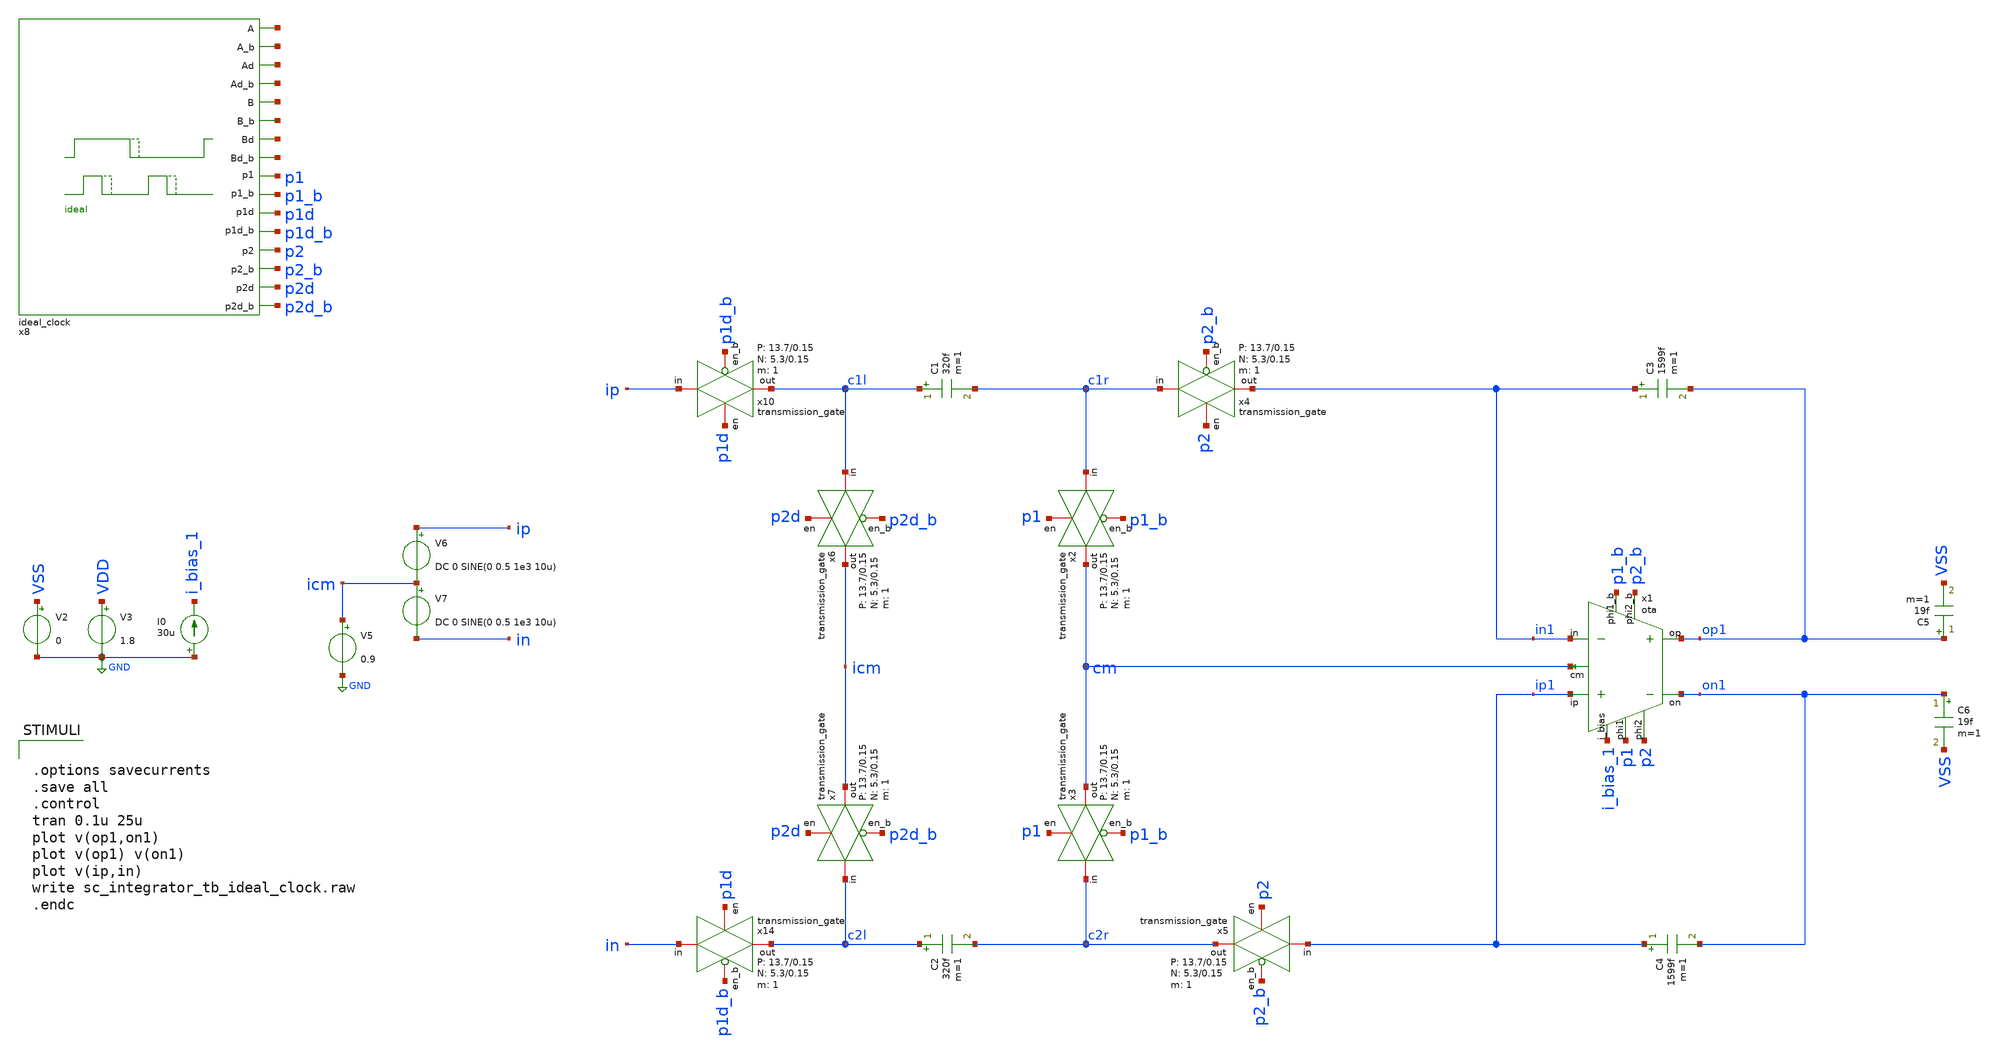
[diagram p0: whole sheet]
** sch_path: verification/analog_modulator/sc_integrator_tb_ideal_clock.sch
**.subckt sc_integrator_tb_ideal_clock
x4 c1r in1 p2 p2_b VDD VSS 1 5.3 0.15 13.7 0.15 transmission_gate
x5 ip1 c2r p2 p2_b VDD VSS 1 5.3 0.15 13.7 0.15 transmission_gate
x2 c1r cm p1 p1_b VDD VSS 1 5.3 0.15 13.7 0.15 transmission_gate
x3 c2r cm p1 p1_b VDD VSS 1 5.3 0.15 13.7 0.15 transmission_gate
C1 c1l c1r 320f m=1
C2 c2l c2r 320f m=1
x10 ip c1l p1d p1d_b VDD VSS 1 5.3 0.15 13.7 0.15 transmission_gate
x14 in c2l p1d p1d_b VDD VSS 1 5.3 0.15 13.7 0.15 transmission_gate
C3 in1 op1 1599f m=1
C4 ip1 on1 1599f m=1
V2 VSS GND 0
V3 VDD GND 1.8
x6 c1l icm p2d p2d_b VDD VSS 1 5.3 0.15 13.7 0.15 transmission_gate
x7 c2l icm p2d p2d_b VDD VSS 1 5.3 0.15 13.7 0.15 transmission_gate
x8 net1 net2 net3 net4 net5 net6 net7 net8 p2 p2_b p2d p2d_b p1d_b p1d p1_b p1 10u VDD VSS
+ ideal_clock
x1 i_bias_1 ip1 in1 p1 p1_b p2 p2_b op1 on1 cm 50 350 VDD VSS ota
I0 GND i_bias_1 30u
C5 op1 VSS 19f m=1
C6 on1 VSS 19f m=1
V5 icm GND 0.9
V6 ip icm DC 0 SINE(0 0.5 1e3 10u)
V7 icm in DC 0 SINE(0 0.5 1e3 10u)
**** begin user architecture code

** opencircuitdesign pdks install
.lib /farmshare/home/classes/ee/372/PDKs/open_pdks_1.0.310/sky130/sky130A/libs.tech/ngspice/sky130.lib.spice tt
.inc /farmshare/home/classes/ee/372/PDKs/open_pdks_1.0.310/sky130/sky130A/libs.ref/sky130_fd_sc_hd/spice/sky130_fd_sc_hd.spice



.options savecurrents
.save all
.control
tran 0.1u 25u
plot v(op1,on1)
plot v(op1) v(on1)
plot v(ip,in)
write sc_integrator_tb_ideal_clock.raw
.endc


**** end user architecture code
**.ends
.GLOBAL GND
.end
